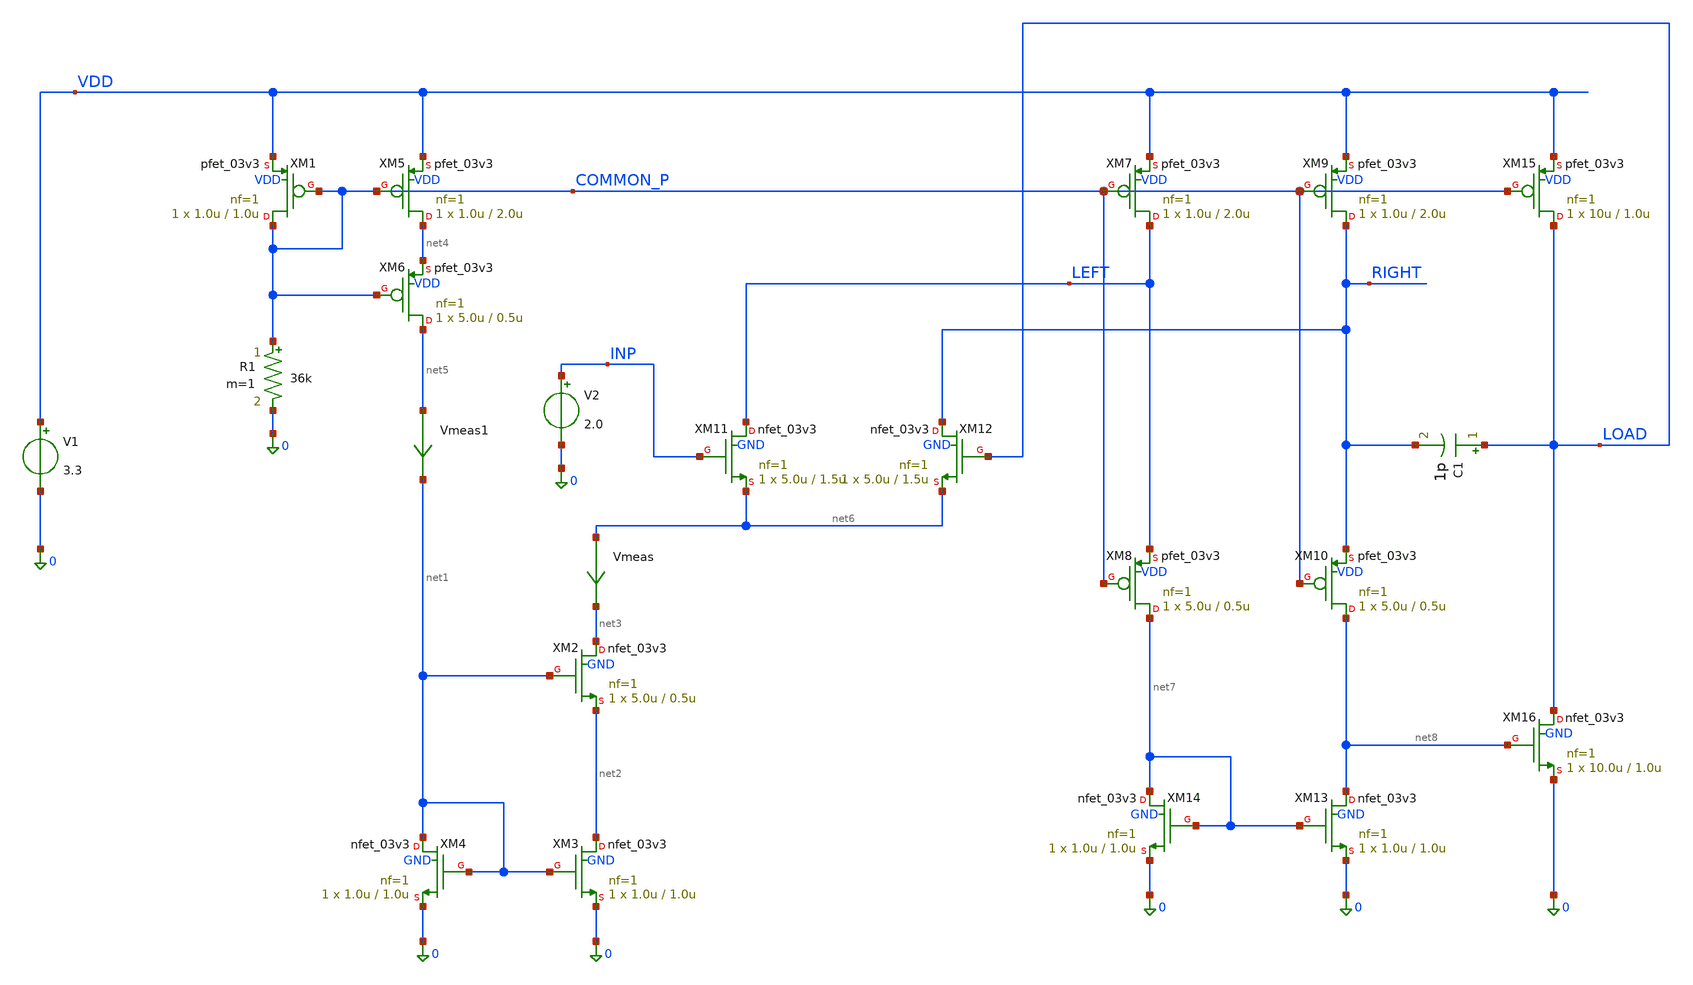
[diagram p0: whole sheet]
** sch_path: xschem/ex_amplifier.sch
**.subckt ex_amplifier
R1 COMMON_P 0 36k m=1
V1 VDD 0 3.3
Vmeas net6 net3 0
XM1 COMMON_P COMMON_P VDD VDD pfet_03v3 L=1.0u W=1.0u nf=1 ad='int((nf+1)/2) * W/nf * 0.18u' as='int((nf+2)/2) * W/nf * 0.18u'
+ pd='2*int((nf+1)/2) * (W/nf + 0.18u)' ps='2*int((nf+2)/2) * (W/nf + 0.18u)' nrd='0.18u / W' nrs='0.18u / W'
+ sa=0 sb=0 sd=0 m=1 par=1
XM2 net3 net1 net2 GND nfet_03v3 L=0.5u W=5.0u nf=1 ad='int((nf+1)/2) * W/nf * 0.18u' as='int((nf+2)/2) * W/nf * 0.18u'
+ pd='2*int((nf+1)/2) * (W/nf + 0.18u)' ps='2*int((nf+2)/2) * (W/nf + 0.18u)' nrd='0.18u / W' nrs='0.18u / W'
+ sa=0 sb=0 sd=0 m=1 par=1
XM3 net2 net1 0 GND nfet_03v3 L=1.0u W=1.0u nf=1 ad='int((nf+1)/2) * W/nf * 0.18u' as='int((nf+2)/2) * W/nf * 0.18u'
+ pd='2*int((nf+1)/2) * (W/nf + 0.18u)' ps='2*int((nf+2)/2) * (W/nf + 0.18u)' nrd='0.18u / W' nrs='0.18u / W'
+ sa=0 sb=0 sd=0 m=1 par=1
XM4 net1 net1 0 GND nfet_03v3 L=1.0u W=1.0u nf=1 ad='int((nf+1)/2) * W/nf * 0.18u' as='int((nf+2)/2) * W/nf * 0.18u'
+ pd='2*int((nf+1)/2) * (W/nf + 0.18u)' ps='2*int((nf+2)/2) * (W/nf + 0.18u)' nrd='0.18u / W' nrs='0.18u / W'
+ sa=0 sb=0 sd=0 m=1 par=1
XM5 net4 COMMON_P VDD VDD pfet_03v3 L=2.0u W=1.0u nf=1 ad='int((nf+1)/2) * W/nf * 0.18u' as='int((nf+2)/2) * W/nf * 0.18u'
+ pd='2*int((nf+1)/2) * (W/nf + 0.18u)' ps='2*int((nf+2)/2) * (W/nf + 0.18u)' nrd='0.18u / W' nrs='0.18u / W'
+ sa=0 sb=0 sd=0 m=1 par=1
XM6 net5 COMMON_P net4 VDD pfet_03v3 L=0.5u W=5.0u nf=1 ad='int((nf+1)/2) * W/nf * 0.18u' as='int((nf+2)/2) * W/nf * 0.18u'
+ pd='2*int((nf+1)/2) * (W/nf + 0.18u)' ps='2*int((nf+2)/2) * (W/nf + 0.18u)' nrd='0.18u / W' nrs='0.18u / W'
+ sa=0 sb=0 sd=0 m=1 par=1
Vmeas1 net5 net1 0
XM7 LEFT COMMON_P VDD VDD pfet_03v3 L=2.0u W=1.0u nf=1 ad='int((nf+1)/2) * W/nf * 0.18u' as='int((nf+2)/2) * W/nf * 0.18u'
+ pd='2*int((nf+1)/2) * (W/nf + 0.18u)' ps='2*int((nf+2)/2) * (W/nf + 0.18u)' nrd='0.18u / W' nrs='0.18u / W'
+ sa=0 sb=0 sd=0 m=1 par=1
XM9 RIGHT COMMON_P VDD VDD pfet_03v3 L=2.0u W=1.0u nf=1 ad='int((nf+1)/2) * W/nf * 0.18u' as='int((nf+2)/2) * W/nf * 0.18u'
+ pd='2*int((nf+1)/2) * (W/nf + 0.18u)' ps='2*int((nf+2)/2) * (W/nf + 0.18u)' nrd='0.18u / W' nrs='0.18u / W'
+ sa=0 sb=0 sd=0 m=1 par=1
XM11 LEFT INP net6 GND nfet_03v3 L=1.5u W=5.0u nf=1 ad='int((nf+1)/2) * W/nf * 0.18u' as='int((nf+2)/2) * W/nf * 0.18u'
+ pd='2*int((nf+1)/2) * (W/nf + 0.18u)' ps='2*int((nf+2)/2) * (W/nf + 0.18u)' nrd='0.18u / W' nrs='0.18u / W'
+ sa=0 sb=0 sd=0 m=1 par=1
XM12 RIGHT LOAD net6 GND nfet_03v3 L=1.5u W=5.0u nf=1 ad='int((nf+1)/2) * W/nf * 0.18u' as='int((nf+2)/2) * W/nf * 0.18u'
+ pd='2*int((nf+1)/2) * (W/nf + 0.18u)' ps='2*int((nf+2)/2) * (W/nf + 0.18u)' nrd='0.18u / W' nrs='0.18u / W'
+ sa=0 sb=0 sd=0 m=1 par=1
V2 INP 0 2.0
XM8 net7 COMMON_P LEFT VDD pfet_03v3 L=0.5u W=5.0u nf=1 ad='int((nf+1)/2) * W/nf * 0.18u' as='int((nf+2)/2) * W/nf * 0.18u'
+ pd='2*int((nf+1)/2) * (W/nf + 0.18u)' ps='2*int((nf+2)/2) * (W/nf + 0.18u)' nrd='0.18u / W' nrs='0.18u / W'
+ sa=0 sb=0 sd=0 m=1 par=1
XM10 net8 COMMON_P RIGHT VDD pfet_03v3 L=0.5u W=5.0u nf=1 ad='int((nf+1)/2) * W/nf * 0.18u' as='int((nf+2)/2) * W/nf * 0.18u'
+ pd='2*int((nf+1)/2) * (W/nf + 0.18u)' ps='2*int((nf+2)/2) * (W/nf + 0.18u)' nrd='0.18u / W' nrs='0.18u / W'
+ sa=0 sb=0 sd=0 m=1 par=1
XM13 net8 net7 0 GND nfet_03v3 L=1.0u W=1.0u nf=1 ad='int((nf+1)/2) * W/nf * 0.18u' as='int((nf+2)/2) * W/nf * 0.18u'
+ pd='2*int((nf+1)/2) * (W/nf + 0.18u)' ps='2*int((nf+2)/2) * (W/nf + 0.18u)' nrd='0.18u / W' nrs='0.18u / W'
+ sa=0 sb=0 sd=0 m=1 par=1
XM14 net7 net7 0 GND nfet_03v3 L=1.0u W=1.0u nf=1 ad='int((nf+1)/2) * W/nf * 0.18u' as='int((nf+2)/2) * W/nf * 0.18u'
+ pd='2*int((nf+1)/2) * (W/nf + 0.18u)' ps='2*int((nf+2)/2) * (W/nf + 0.18u)' nrd='0.18u / W' nrs='0.18u / W'
+ sa=0 sb=0 sd=0 m=1 par=1
XM15 LOAD COMMON_P VDD VDD pfet_03v3 L=1.0u W=10u nf=1 ad='int((nf+1)/2) * W/nf * 0.18u' as='int((nf+2)/2) * W/nf * 0.18u'
+ pd='2*int((nf+1)/2) * (W/nf + 0.18u)' ps='2*int((nf+2)/2) * (W/nf + 0.18u)' nrd='0.18u / W' nrs='0.18u / W'
+ sa=0 sb=0 sd=0 m=1 par=1
XM16 LOAD net8 0 GND nfet_03v3 L=1.0u W=10.0u nf=1 ad='int((nf+1)/2) * W/nf * 0.18u' as='int((nf+2)/2) * W/nf * 0.18u'
+ pd='2*int((nf+1)/2) * (W/nf + 0.18u)' ps='2*int((nf+2)/2) * (W/nf + 0.18u)' nrd='0.18u / W' nrs='0.18u / W'
+ sa=0 sb=0 sd=0 m=1 par=1
C1 LOAD RIGHT 1p m=1
**** begin user architecture code

.include $::180MCU_MODELS/design.ngspice
.lib $::180MCU_MODELS/sm141064.ngspice typical
.lib $::180MCU_MODELS/sm141064.ngspice res_typical
.lib $::180MCU_MODELS/sm141064.ngspice moscap_typical
.lib $::180MCU_MODELS/sm141064.ngspice diode_typical
* .lib $::180MCU_MODELS/sm141064.ngspice res_statistical




.control
	tran 25n 1m
	save all
	write ex_amplifier.raw
	quit
.endc



**** end user architecture code
**.ends
.end
